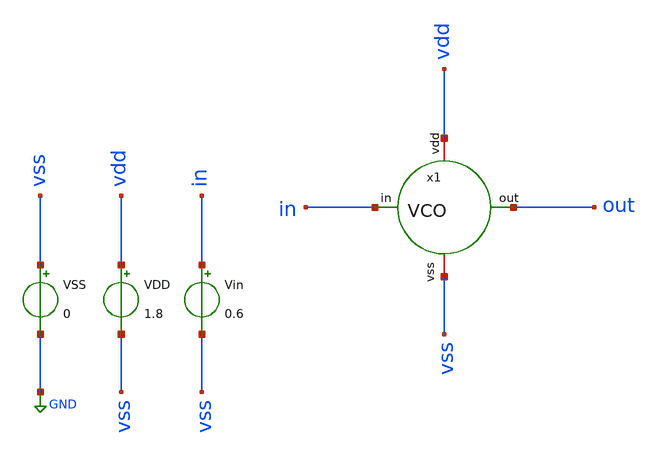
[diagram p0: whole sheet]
** sch_path: sch/PLL_caravel/tb_VCO.sch
**.subckt tb_VCO
VSS vss GND 0
VDD vdd vss 1.8
Vin in vss 0.6
x1 vdd out in vss VCO
**** begin user architecture code



* Parameters
.options TEMPS = 27.0

* Models
.lib ~/skywater/skywater-pdk/libraries/sky130_fd_pr_ngspice/latest/models/corners/sky130.lib TT

* Data to save
.save all

* Simulation
.control
	tran 0.1ns 0.5us
        setplot tran1
        plot v(in) v(out)
        set filetype = ascii
        write VCO_tran.raw
.endc

.end


**** end user architecture code
**.ends

* expanding   symbol:  PLL_caravel/VCO.sym # of pins=4
** sym_path: sch/PLL_caravel/VCO.sym
** sch_path: sch/PLL_caravel/VCO.sch
.subckt VCO vdd out in vss
*.iopin vdd
*.iopin vss
*.ipin in
*.opin out
x1 vdd_ro ring_out o1 vss_ro NOT
x2 vdd_ro o1 o2 vss_ro NOT
x3 vdd_ro o2 o3 vss_ro NOT
x4 vdd_ro o3 o4 vss_ro NOT
x5 vdd_ro o4 o5 vss_ro NOT
x6 vdd_ro o5 o6 vss_ro NOT
XM1 vdd_ro pol vdd vdd sky130_fd_pr__pfet_01v8 L=0.15 W=1.08 nf=1 ad='int((nf+1)/2) * W/nf * 0.29' as='int((nf+2)/2) * W/nf * 0.29'
+ pd='2*int((nf+1)/2) * (W/nf + 0.29)' ps='2*int((nf+2)/2) * (W/nf + 0.29)' nrd='0.29 / W' nrs='0.29 / W'
+ sa=0 sb=0 sd=0 mult=1 m=1
XM2 vss_ro in vss vss sky130_fd_pr__nfet_01v8 L=0.15 W=1.08 nf=1 ad='int((nf+1)/2) * W/nf * 0.29' as='int((nf+2)/2) * W/nf * 0.29'
+ pd='2*int((nf+1)/2) * (W/nf + 0.29)' ps='2*int((nf+2)/2) * (W/nf + 0.29)' nrd='0.29 / W' nrs='0.29 / W'
+ sa=0 sb=0 sd=0 mult=1 m=1
XM3 pol pol vdd vdd sky130_fd_pr__pfet_01v8 L=0.15 W=0.84 nf=1 ad='int((nf+1)/2) * W/nf * 0.29' as='int((nf+2)/2) * W/nf * 0.29'
+ pd='2*int((nf+1)/2) * (W/nf + 0.29)' ps='2*int((nf+2)/2) * (W/nf + 0.29)' nrd='0.29 / W' nrs='0.29 / W'
+ sa=0 sb=0 sd=0 mult=1 m=1
XM4 vss in pol vss sky130_fd_pr__nfet_01v8 L=0.15 W=0.84 nf=1 ad='int((nf+1)/2) * W/nf * 0.29' as='int((nf+2)/2) * W/nf * 0.29'
+ pd='2*int((nf+1)/2) * (W/nf + 0.29)' ps='2*int((nf+2)/2) * (W/nf + 0.29)' nrd='0.29 / W' nrs='0.29 / W'
+ sa=0 sb=0 sd=0 mult=1 m=1
XM5 out ring_out vdd vdd sky130_fd_pr__pfet_01v8 L=0.15 W=1.08 nf=1 ad='int((nf+1)/2) * W/nf * 0.29'
+ as='int((nf+2)/2) * W/nf * 0.29' pd='2*int((nf+1)/2) * (W/nf + 0.29)' ps='2*int((nf+2)/2) * (W/nf + 0.29)'
+ nrd='0.29 / W' nrs='0.29 / W' sa=0 sb=0 sd=0 mult=1 m=1
XM6 out ring_out vss vss sky130_fd_pr__nfet_01v8 L=0.15 W=0.54 nf=1 ad='int((nf+1)/2) * W/nf * 0.29'
+ as='int((nf+2)/2) * W/nf * 0.29' pd='2*int((nf+1)/2) * (W/nf + 0.29)' ps='2*int((nf+2)/2) * (W/nf + 0.29)'
+ nrd='0.29 / W' nrs='0.29 / W' sa=0 sb=0 sd=0 mult=1 m=1
XM7 ring_out o6 vdd_ro vdd_ro sky130_fd_pr__pfet_01v8 L=0.15 W=2.4 nf=1 ad='int((nf+1)/2) * W/nf * 0.29'
+ as='int((nf+2)/2) * W/nf * 0.29' pd='2*int((nf+1)/2) * (W/nf + 0.29)' ps='2*int((nf+2)/2) * (W/nf + 0.29)'
+ nrd='0.29 / W' nrs='0.29 / W' sa=0 sb=0 sd=0 mult=1 m=1
XM8 ring_out o6 vss_ro vss_ro sky130_fd_pr__nfet_01v8 L=0.15 W=1.2 nf=1 ad='int((nf+1)/2) * W/nf * 0.29'
+ as='int((nf+2)/2) * W/nf * 0.29' pd='2*int((nf+1)/2) * (W/nf + 0.29)' ps='2*int((nf+2)/2) * (W/nf + 0.29)'
+ nrd='0.29 / W' nrs='0.29 / W' sa=0 sb=0 sd=0 mult=1 m=1
.ends


* expanding   symbol:  PLL_caravel/NOT.sym # of pins=4
** sym_path: sch/PLL_caravel/NOT.sym
** sch_path: sch/PLL_caravel/NOT.sch
.subckt NOT vdd in out vss
*.iopin vdd
*.iopin vss
*.ipin in
*.opin out
XM1 out in vdd vdd sky130_fd_pr__pfet_01v8 L=0.15 W=0.84 nf=1 ad='int((nf+1)/2) * W/nf * 0.29' as='int((nf+2)/2) * W/nf * 0.29'
+ pd='2*int((nf+1)/2) * (W/nf + 0.29)' ps='2*int((nf+2)/2) * (W/nf + 0.29)' nrd='0.29 / W' nrs='0.29 / W'
+ sa=0 sb=0 sd=0 mult=1 m=1
XM2 out in vss vss sky130_fd_pr__nfet_01v8 L=0.15 W=0.42 nf=1 ad='int((nf+1)/2) * W/nf * 0.29' as='int((nf+2)/2) * W/nf * 0.29'
+ pd='2*int((nf+1)/2) * (W/nf + 0.29)' ps='2*int((nf+2)/2) * (W/nf + 0.29)' nrd='0.29 / W' nrs='0.29 / W'
+ sa=0 sb=0 sd=0 mult=1 m=1
.ends

.GLOBAL GND
.end
